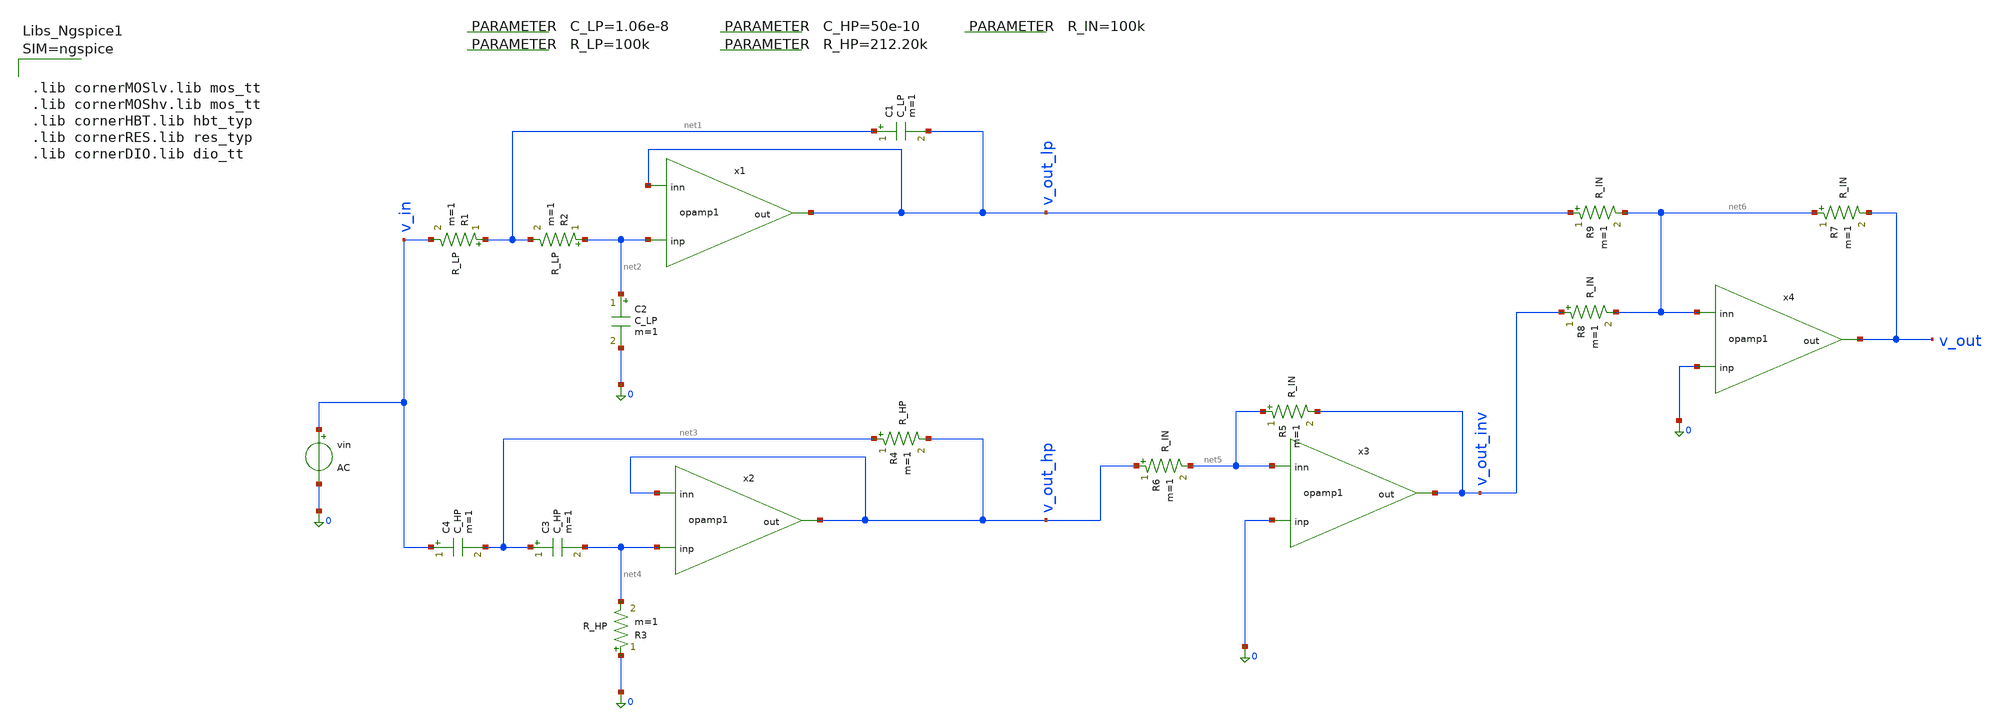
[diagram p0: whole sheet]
** sch_path: 003_Ideal_Circuits/linkwitz_riley_cross_opamo_150hz.sch
**.subckt linkwitz_riley_cross_opamo_150hz
R1 net1 v_in R_LP m=1
R2 net2 net1 R_LP m=1
C1 net1 v_out_lp C_LP m=1
C2 net2 0 C_LP m=1
vin v_in 0 AC
R3 0 net4 R_HP m=1
R4 net3 v_out_hp R_HP m=1
C3 net3 net4 C_HP m=1
C4 v_in net3 C_HP m=1
R5 net5 v_out_inv R_IN m=1
R6 v_out_hp net5 R_IN m=1
R7 net6 v_out R_IN m=1
R8 v_out_inv net6 R_IN m=1
R9 v_out_lp net6 R_IN m=1
x1 net2 v_out_lp v_out_lp opamp1
x2 net4 v_out_hp v_out_hp opamp1
x3 0 net5 v_out_inv opamp1
x4 0 net6 v_out opamp1
.param C_LP=1.06e-8
.param R_LP=100k
.param C_HP=50e-10
.param R_HP=212.20k
.param R_IN=100k
**** begin user architecture code



.lib cornerMOSlv.lib mos_tt
.lib cornerMOShv.lib mos_tt
.lib cornerHBT.lib hbt_typ
.lib cornerRES.lib res_typ
.lib cornerDIO.lib dio_tt






.ac dec 10 1 100k
.save all
.control
run
*plot v_out
plot db(v_out_lp/v_in) db(v_out_hp/v_in) db(v_out/v_in)

.endc



**** end user architecture code
**.ends

* expanding   symbol:  001_provided_files/2_Idealized_circuits/opamp1.sym # of pins=3
** sym_path: 001_provided_files/2_Idealized_circuits/opamp1.sym
** sch_path: 001_provided_files/2_Idealized_circuits/opamp1.sch
.subckt opamp1 inp inn out
*.ipin inp
*.ipin inn
*.opin out
Rin inp inn 10MEG m=1
Rout net2 out 10 m=1
Cp net1 GND 1.59u m=1
Rp GND net1 1k m=1
Ebuf net2 GND net1 GND 1
G1 net1 GND inp inn 1
.ends

.GLOBAL GND
.end
